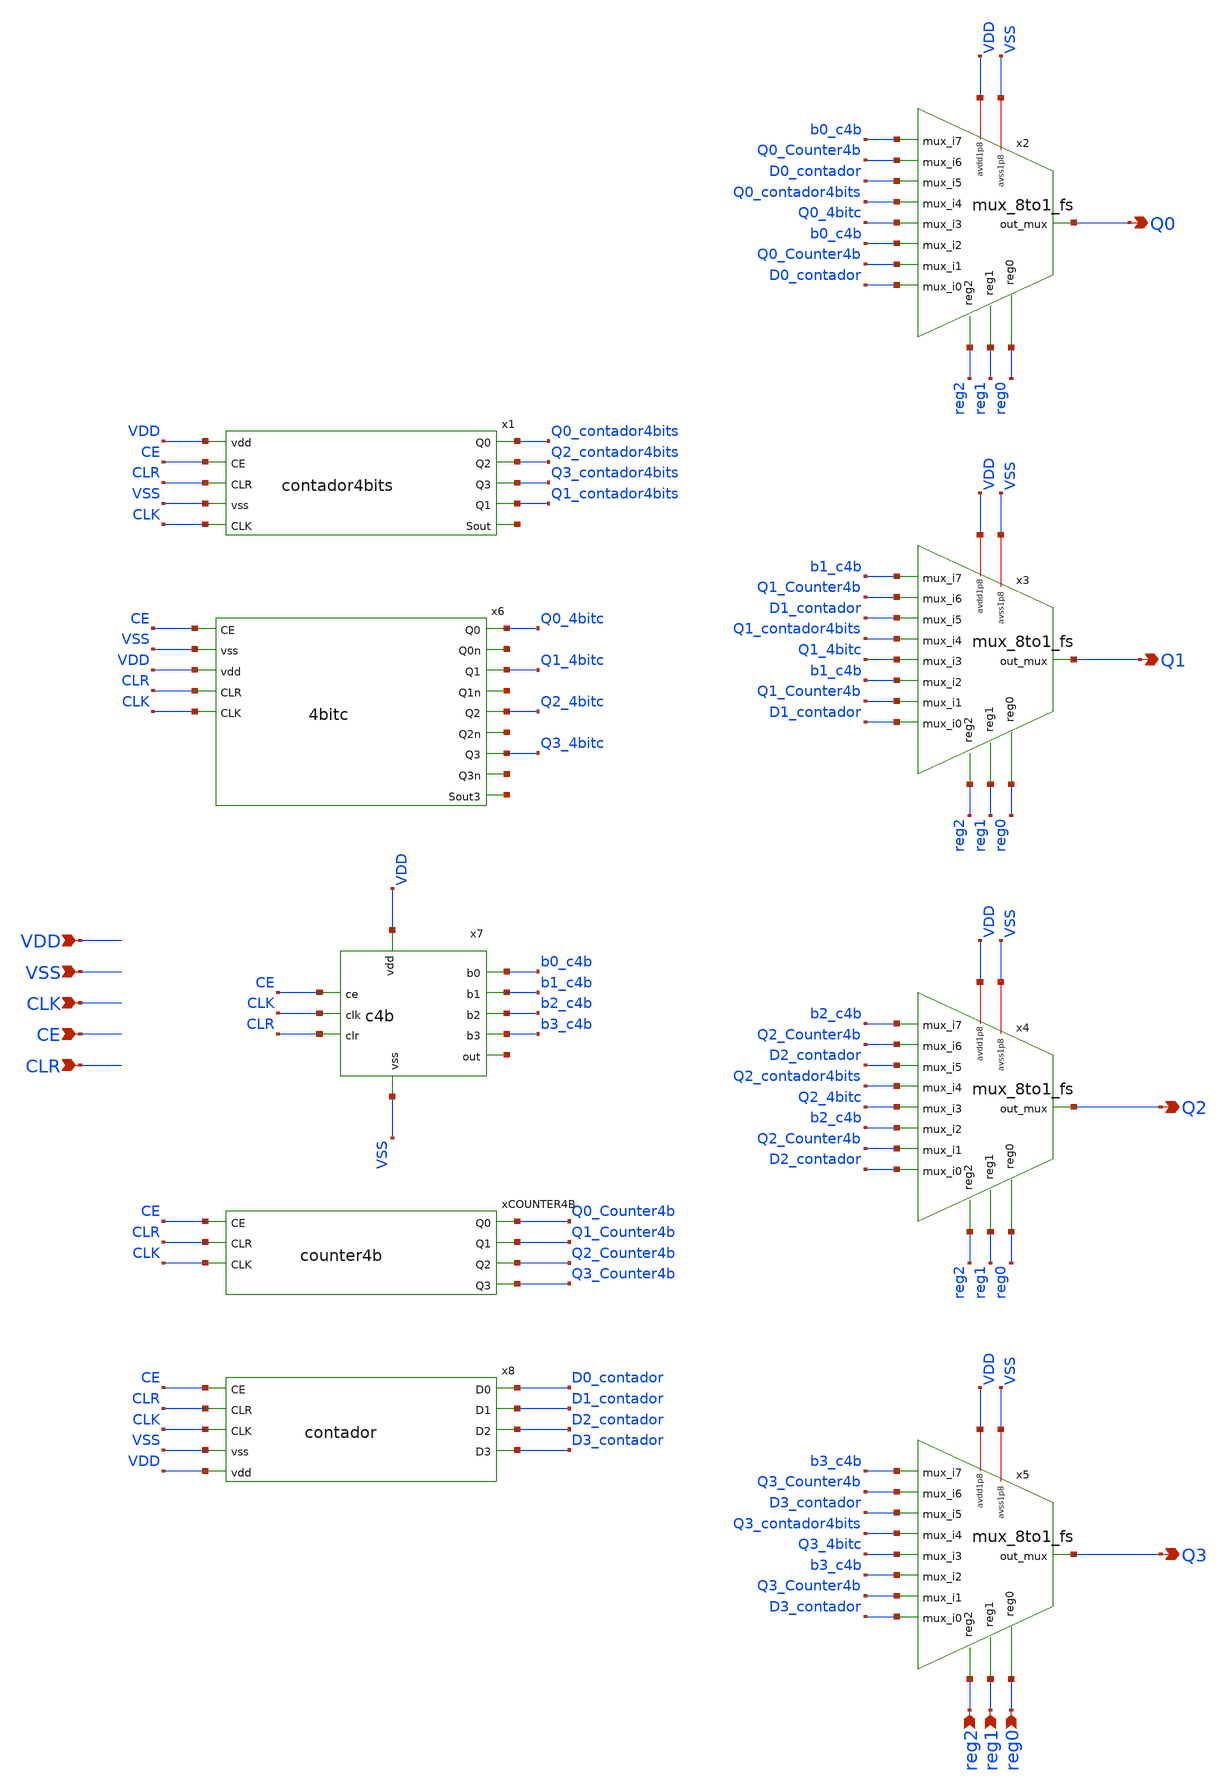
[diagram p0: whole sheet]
** sch_path: track_vlsi/toplevel_vlsi/sch/toplevel.sch
**.subckt toplevel VDD VSS CLK CE CLR reg2 reg1 reg0 Q0 Q1 Q2 Q3
*.ipin VDD
*.ipin VSS
*.ipin CLK
*.ipin CE
*.ipin CLR
*.ipin reg2
*.ipin reg1
*.ipin reg0
*.opin Q0
*.opin Q1
*.opin Q2
*.opin Q3
x2 VDD VSS b0_c4b Q0_Counter4b D0_contador Q0 Q0_contador4bits Q0_4bitc reg0 b0_c4b Q0_Counter4b
+ D0_contador reg1 reg2 mux_8to1_fs
x3 VDD VSS b1_c4b Q1_Counter4b D1_contador Q1 Q1_contador4bits Q1_4bitc reg0 b1_c4b Q1_Counter4b
+ D1_contador reg1 reg2 mux_8to1_fs
x4 VDD VSS b2_c4b Q2_Counter4b D2_contador Q2 Q2_contador4bits Q2_4bitc reg0 b2_c4b Q2_Counter4b
+ D2_contador reg1 reg2 mux_8to1_fs
x5 VDD VSS b3_c4b Q3_Counter4b D3_contador Q3 Q3_contador4bits Q3_4bitc reg0 b3_c4b Q3_Counter4b
+ D3_contador reg1 reg2 mux_8to1_fs
x6 Q0_4bitc CE net1 Q1_4bitc net2 Q2_4bitc net3 Q3_4bitc net4 net5 VSS VDD CLR CLK 4bitc
x7 CE CLK CLR VDD VSS b0_c4b b1_c4b b2_c4b b3_c4b net6 c4b
xCOUNTER4B CE Q0_Counter4b CLR CLK Q1_Counter4b Q2_Counter4b Q3_Counter4b VSS VDD counter4b
x8 D0_contador CE CLR CLK VSS VDD D1_contador D2_contador D3_contador contador
x1 VDD Q0_contador4bits Q2_contador4bits Q3_contador4bits Q1_contador4bits CE CLR net7 VSS CLK
+ contador4bits
**.ends
.end
